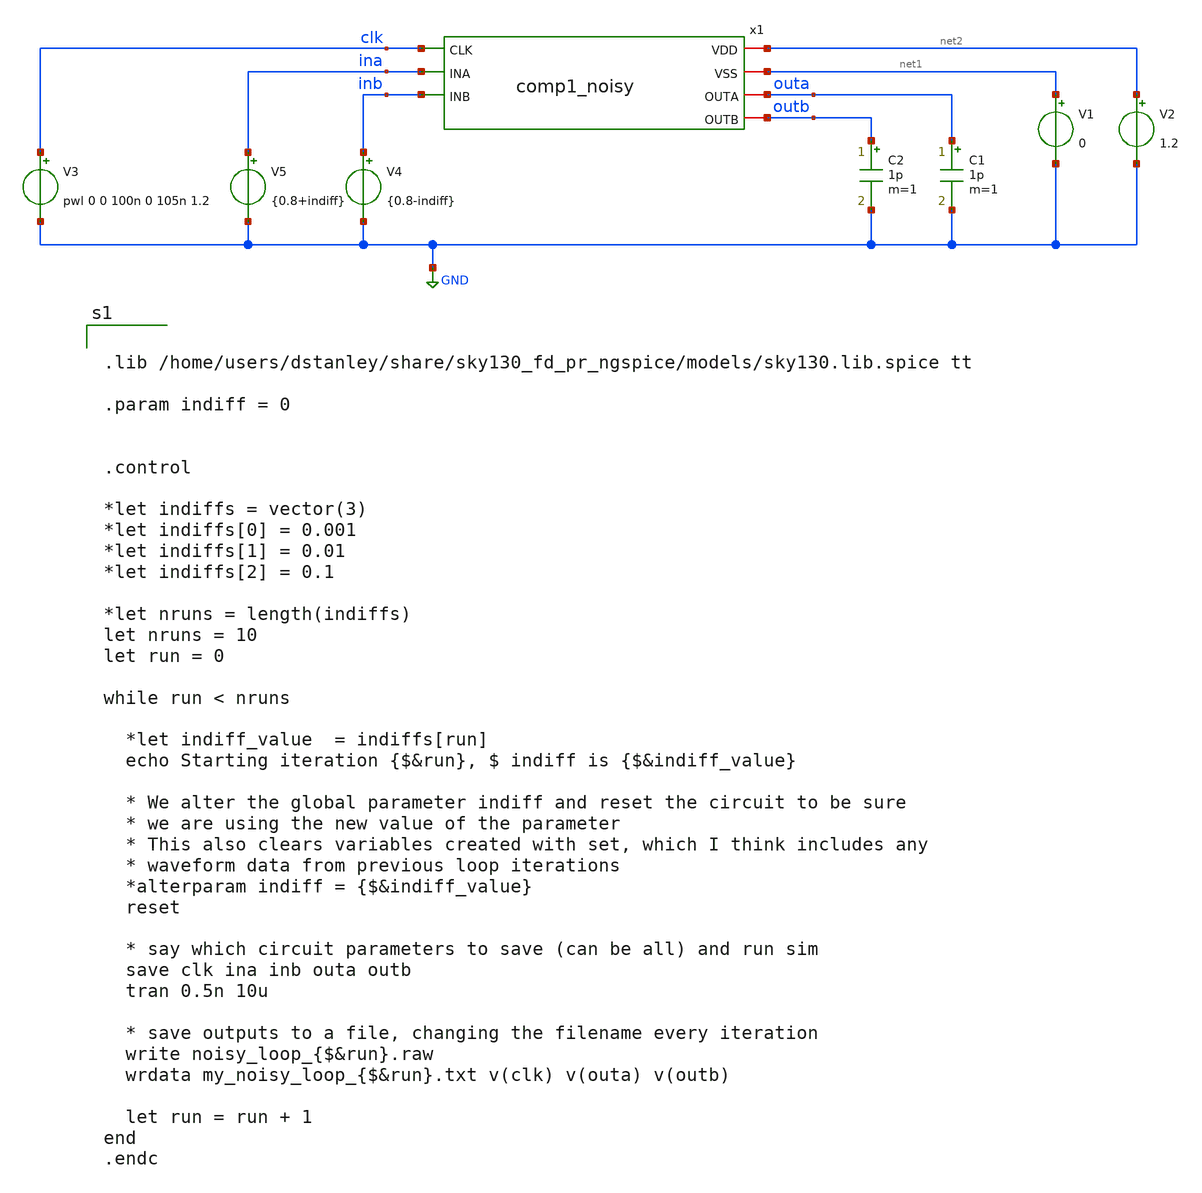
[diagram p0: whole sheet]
** sch_path: comp1_loop_test_noise.sch
**.subckt comp1_loop_test_noise
V1 net1 GND 0
V2 net2 GND 1.2
C1 outa GND 1p m=1
C2 outb GND 1p m=1
V3 clk GND pwl 0 0 100n 0 105n 1.2
V4 inb GND {0.8-indiff}
V5 ina GND {0.8+indiff}
x1 net2 net1 clk ina inb outa outb comp1_noisy
**** begin user architecture code


.lib /home/users/dstanley/share/sky130_fd_pr_ngspice/models/sky130.lib.spice tt

.param indiff = 0


.control

*let indiffs = vector(3)
*let indiffs[0] = 0.001
*let indiffs[1] = 0.01
*let indiffs[2] = 0.1

*let nruns = length(indiffs)
let nruns = 10
let run = 0

while run < nruns

  *let indiff_value  = indiffs[run]
  echo Starting iteration {$&run}, $ indiff is {$&indiff_value}

  * We alter the global parameter indiff and reset the circuit to be sure
  * we are using the new value of the parameter
  * This also clears variables created with set, which I think includes any
  * waveform data from previous loop iterations
  *alterparam indiff = {$&indiff_value}
  reset

  * say which circuit parameters to save (can be all) and run sim
  save clk ina inb outa outb
  tran 0.5n 10u

  * save outputs to a file, changing the filename every iteration
  write noisy_loop_{$&run}.raw
  wrdata my_noisy_loop_{$&run}.txt v(clk) v(outa) v(outb)

  let run = run + 1
end
.endc


**** end user architecture code
**.ends

* expanding   symbol:  /home/users/dstanley/EE272B/xschem_tests/comp1_noisy.sym # of pins=7
** sym_path: comp1_noisy.sym
** sch_path: comp1_noisy.sch
.subckt comp1_noisy VDD VSS CLK INA INB OUTA OUTB
*.iopin VSS
*.iopin VDD
*.iopin OUTB
*.iopin OUTA
*.ipin INB
*.ipin INA
*.ipin CLK
XM1 net2 CLK VSS VSS sky130_fd_pr__nfet_01v8 L=0.15 W=1 nf=1 ad='int((nf+1)/2) * W/nf * 0.29' as='int((nf+2)/2) * W/nf * 0.29'
+ pd='2*int((nf+1)/2) * (W/nf + 0.29)' ps='2*int((nf+2)/2) * (W/nf + 0.29)' nrd='0.29 / W' nrs='0.29 / W'
+ sa=0 sb=0 sd=0 mult=1 m=1
XM2 net1 INA net2 VSS sky130_fd_pr__nfet_01v8 L=0.15 W=1 nf=1 ad='int((nf+1)/2) * W/nf * 0.29' as='int((nf+2)/2) * W/nf * 0.29'
+ pd='2*int((nf+1)/2) * (W/nf + 0.29)' ps='2*int((nf+2)/2) * (W/nf + 0.29)' nrd='0.29 / W' nrs='0.29 / W'
+ sa=0 sb=0 sd=0 mult=1 m=1
XM5 OUTB OUTA VDD VDD sky130_fd_pr__pfet_01v8 L=0.15 W=1 nf=1 ad='int((nf+1)/2) * W/nf * 0.29' as='int((nf+2)/2) * W/nf * 0.29'
+ pd='2*int((nf+1)/2) * (W/nf + 0.29)' ps='2*int((nf+2)/2) * (W/nf + 0.29)' nrd='0.29 / W' nrs='0.29 / W'
+ sa=0 sb=0 sd=0 mult=1 m=1
XM6 OUTB CLK VDD VDD sky130_fd_pr__pfet_01v8 L=0.15 W=1 nf=1 ad='int((nf+1)/2) * W/nf * 0.29' as='int((nf+2)/2) * W/nf * 0.29'
+ pd='2*int((nf+1)/2) * (W/nf + 0.29)' ps='2*int((nf+2)/2) * (W/nf + 0.29)' nrd='0.29 / W' nrs='0.29 / W'
+ sa=0 sb=0 sd=0 mult=1 m=1
XM3 net3 INB net2 VSS sky130_fd_pr__nfet_01v8 L=0.15 W=1 nf=1 ad='int((nf+1)/2) * W/nf * 0.29' as='int((nf+2)/2) * W/nf * 0.29'
+ pd='2*int((nf+1)/2) * (W/nf + 0.29)' ps='2*int((nf+2)/2) * (W/nf + 0.29)' nrd='0.29 / W' nrs='0.29 / W'
+ sa=0 sb=0 sd=0 mult=1 m=1
XM8 OUTA OUTB VDD VDD sky130_fd_pr__pfet_01v8 L=0.15 W=1 nf=1 ad='int((nf+1)/2) * W/nf * 0.29' as='int((nf+2)/2) * W/nf * 0.29'
+ pd='2*int((nf+1)/2) * (W/nf + 0.29)' ps='2*int((nf+2)/2) * (W/nf + 0.29)' nrd='0.29 / W' nrs='0.29 / W'
+ sa=0 sb=0 sd=0 mult=1 m=1
XM9 OUTA CLK VDD VDD sky130_fd_pr__pfet_01v8 L=0.15 W=1 nf=1 ad='int((nf+1)/2) * W/nf * 0.29' as='int((nf+2)/2) * W/nf * 0.29'
+ pd='2*int((nf+1)/2) * (W/nf + 0.29)' ps='2*int((nf+2)/2) * (W/nf + 0.29)' nrd='0.29 / W' nrs='0.29 / W'
+ sa=0 sb=0 sd=0 mult=1 m=1
x1 VSS OUTB OUTA net1 nmos_noisy
x2 VSS OUTA OUTB net3 nmos_noisy
.ends


* expanding   symbol:  /home/users/dstanley/EE272B/xschem_tests/nmos_noisy.sym # of pins=4
** sym_path: nmos_noisy.sym
** sch_path: nmos_noisy.sch
.subckt nmos_noisy B D G S
*.iopin S
*.ipin G
*.iopin D
*.ipin B
XM1 net1 G S B sky130_fd_pr__nfet_01v8 L=0.15 W=1 nf=1 ad='int((nf+1)/2) * W/nf * 0.29' as='int((nf+2)/2) * W/nf * 0.29'
+ pd='2*int((nf+1)/2) * (W/nf + 0.29)' ps='2*int((nf+2)/2) * (W/nf + 0.29)' nrd='0.29 / W' nrs='0.29 / W'
+ sa=0 sb=0 sd=0 mult=1 m=1
V1 noise_node S DC 0 trnoise(0 {noise_timestep} {oneoverf_exponent} {oneoverf_rms})
**** begin user architecture code

.param noise_max_freq=100MEG
.param noise_timestep={1/noise_max_freq}
.param oneoverf_exponent=0.8
.param oneoverf_rms=6.63n
.param i_nominal=14.46u

**** end user architecture code
B1 D S I = i(V2)/{i_nominal}*v(noise_node, S)
V2 D net1 dc 0
R1 noise_node S 1k m=1
.ends

.GLOBAL GND
.end
